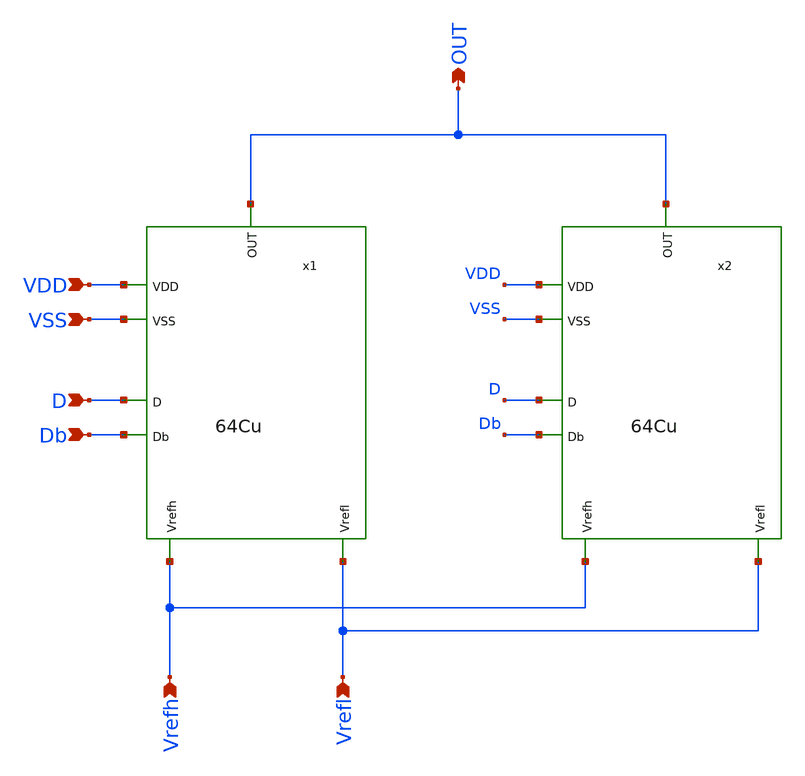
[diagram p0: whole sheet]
** sch_path: 128Cu.sch
**.subckt 128Cu OUT VDD D VSS Vrefh Vrefl Db
*.opin OUT
*.ipin VDD
*.ipin D
*.ipin VSS
*.ipin Vrefh
*.ipin Vrefl
*.ipin Db
x1 OUT VSS VDD Db D Vrefl Vrefh 64Cu
x2 OUT VSS VDD Db D Vrefl Vrefh 64Cu
**.ends
.end
